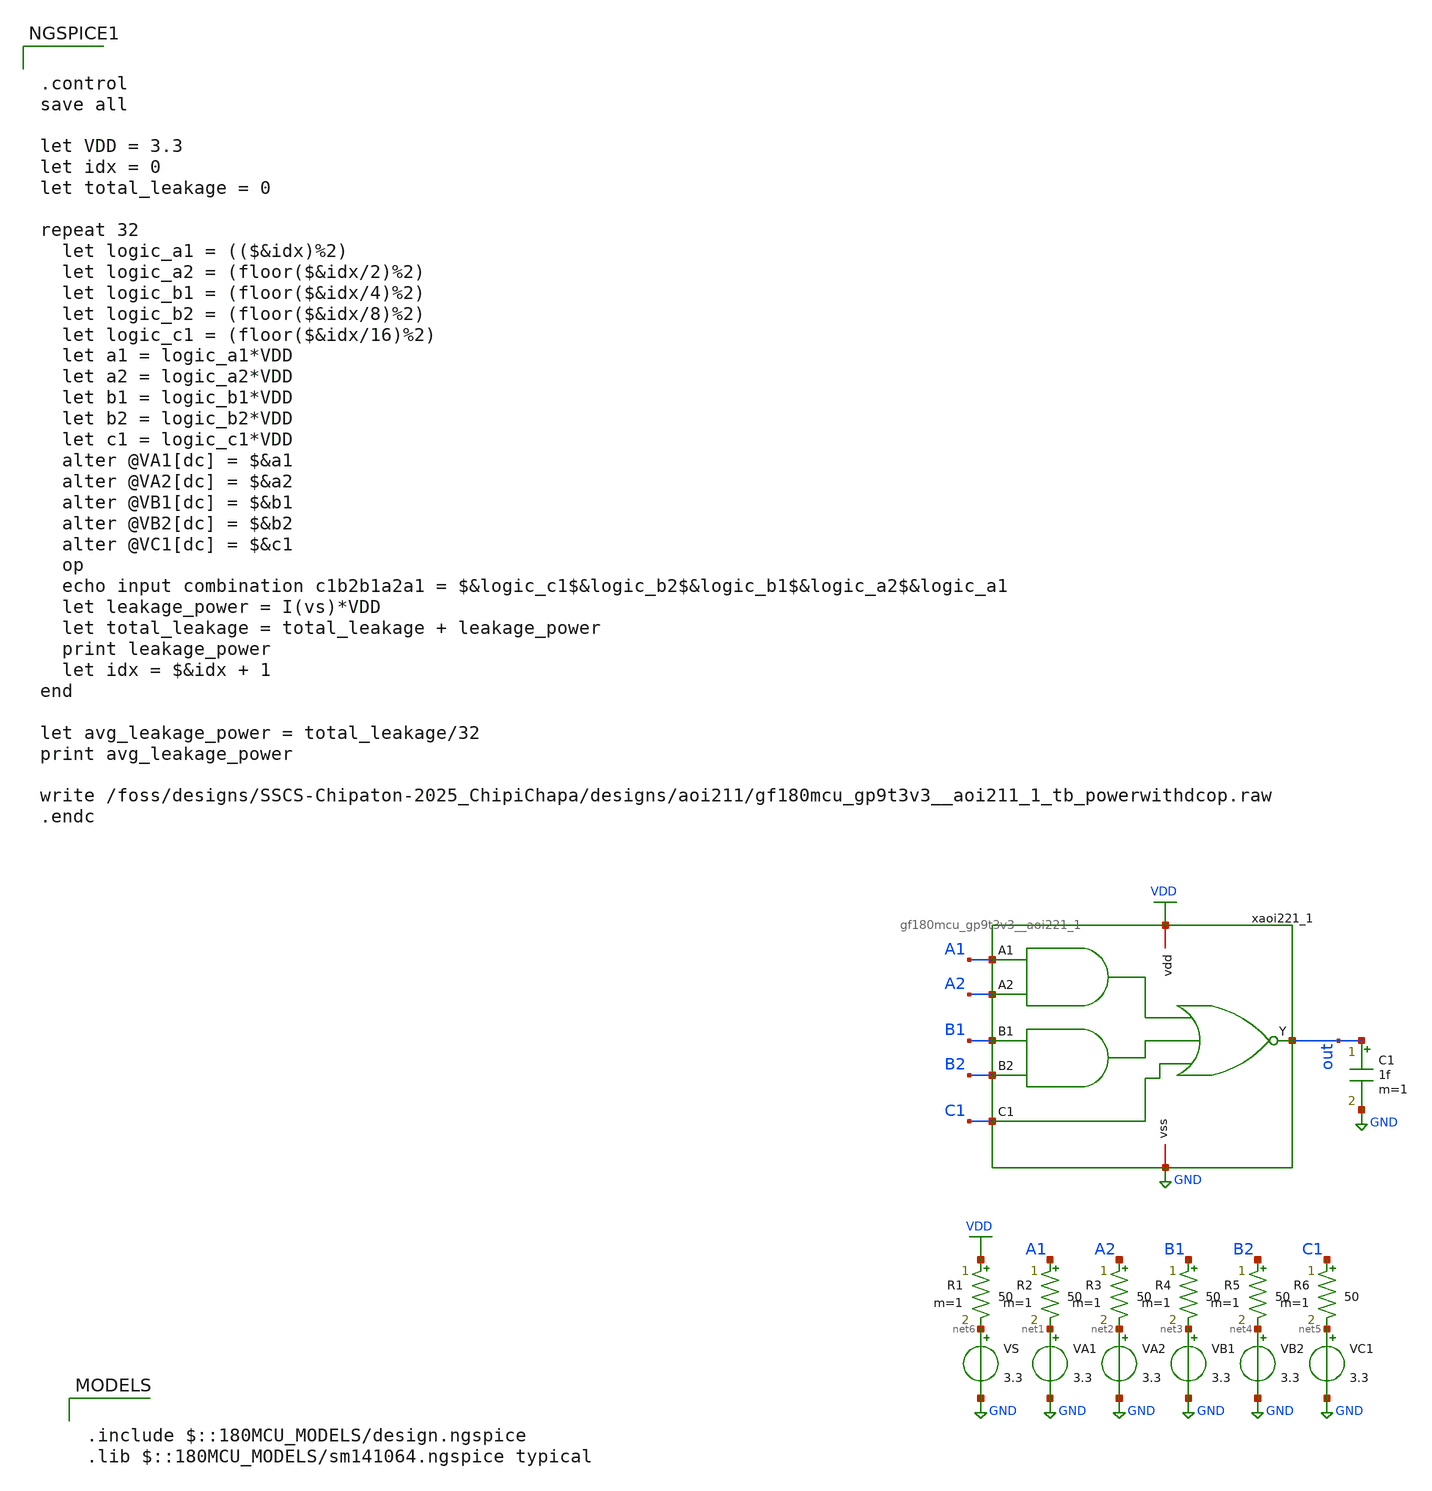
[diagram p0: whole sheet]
** sch_path: designs/aoi221/gf180mcu_gp9t3v3__aoi221_1_tb_power_with_dc_op.sch
**.subckt gf180mcu_gp9t3v3__aoi221_1_tb_power_with_dc_op
VA1 net1 GND 3.3
VA2 net2 GND 3.3
VB1 net3 GND 3.3
VB2 net4 GND 3.3
VC1 net5 GND 3.3
VS net6 GND 3.3
xaoi221_1 VDD out B1 A1 C1 B2 A2 GND gf180mcu_gp9t3v3__aoi221_1
C1 out GND 1f m=1
R1 VDD net6 50 m=1
R2 A1 net1 50 m=1
R3 A2 net2 50 m=1
R4 B1 net3 50 m=1
R5 B2 net4 50 m=1
R6 C1 net5 50 m=1
**** begin user architecture code

.include $::180MCU_MODELS/design.ngspice
.lib $::180MCU_MODELS/sm141064.ngspice typical



.control
save all

let VDD = 3.3
let idx = 0
let total_leakage = 0

repeat 32
  let logic_a1 = (($&idx)%2)
  let logic_a2 = (floor($&idx/2)%2)
  let logic_b1 = (floor($&idx/4)%2)
  let logic_b2 = (floor($&idx/8)%2)
  let logic_c1 = (floor($&idx/16)%2)
  let a1 = logic_a1*VDD
  let a2 = logic_a2*VDD
  let b1 = logic_b1*VDD
  let b2 = logic_b2*VDD
  let c1 = logic_c1*VDD
  alter @VA1[dc] = $&a1
  alter @VA2[dc] = $&a2
  alter @VB1[dc] = $&b1
  alter @VB2[dc] = $&b2
  alter @VC1[dc] = $&c1
  op
  echo input combination c1b2b1a2a1 = $&logic_c1$&logic_b2$&logic_b1$&logic_a2$&logic_a1
  let leakage_power = I(vs)*VDD
  let total_leakage = total_leakage + leakage_power
  print leakage_power
  let idx = $&idx + 1
end

let avg_leakage_power = total_leakage/32
print avg_leakage_power

write
+ /foss/designs/SSCS-Chipaton-2025_ChipiChapa/designs/aoi211/gf180mcu_gp9t3v3__aoi211_1_tb_powerwithdcop.raw
.endc


**** end user architecture code
**.ends

* expanding   symbol:  gf180mcu_gp9t3v3__aoi221_1.sym # of pins=8
** sym_path: designs/aoi221/gf180mcu_gp9t3v3__aoi221_1.sym
** sch_path: designs/aoi221/gf180mcu_gp9t3v3__aoi221_1.sch
.subckt gf180mcu_gp9t3v3__aoi221_1 vdd Y B1 A1 C1 B2 A2 vss
*.iopin vdd
*.iopin vss
*.ipin A1
*.ipin A2
*.ipin B2
*.ipin B1
*.ipin C1
*.opin Y
XM1 Y A1 net1 vss nfet_03v3 L=0.3u W=1u nf=1 ad='int((nf+1)/2) * W/nf * 0.18u' as='int((nf+2)/2) * W/nf * 0.18u'
+ pd='2*int((nf+1)/2) * (W/nf + 0.18u)' ps='2*int((nf+2)/2) * (W/nf + 0.18u)' nrd='0.18u / W' nrs='0.18u / W'
+ sa=0 sb=0 sd=0 m=1
XM2 net1 A2 vss vss nfet_03v3 L=0.3u W=1u nf=1 ad='int((nf+1)/2) * W/nf * 0.18u' as='int((nf+2)/2) * W/nf * 0.18u'
+ pd='2*int((nf+1)/2) * (W/nf + 0.18u)' ps='2*int((nf+2)/2) * (W/nf + 0.18u)' nrd='0.18u / W' nrs='0.18u / W'
+ sa=0 sb=0 sd=0 m=1
XM3 Y B1 net2 vss nfet_03v3 L=0.3u W=1u nf=1 ad='int((nf+1)/2) * W/nf * 0.18u' as='int((nf+2)/2) * W/nf * 0.18u'
+ pd='2*int((nf+1)/2) * (W/nf + 0.18u)' ps='2*int((nf+2)/2) * (W/nf + 0.18u)' nrd='0.18u / W' nrs='0.18u / W'
+ sa=0 sb=0 sd=0 m=1
XM4 net2 B2 vss vss nfet_03v3 L=0.3u W=1u nf=1 ad='int((nf+1)/2) * W/nf * 0.18u' as='int((nf+2)/2) * W/nf * 0.18u'
+ pd='2*int((nf+1)/2) * (W/nf + 0.18u)' ps='2*int((nf+2)/2) * (W/nf + 0.18u)' nrd='0.18u / W' nrs='0.18u / W'
+ sa=0 sb=0 sd=0 m=1
XM5 Y C1 vss vss nfet_03v3 L=0.3u W=0.5u nf=1 ad='int((nf+1)/2) * W/nf * 0.18u' as='int((nf+2)/2) * W/nf * 0.18u'
+ pd='2*int((nf+1)/2) * (W/nf + 0.18u)' ps='2*int((nf+2)/2) * (W/nf + 0.18u)' nrd='0.18u / W' nrs='0.18u / W'
+ sa=0 sb=0 sd=0 m=1
XM6 net4 A1 vdd vdd pfet_03v3 L=0.3u W=2.25u nf=1 ad='int((nf+1)/2) * W/nf * 0.18u' as='int((nf+2)/2) * W/nf * 0.18u'
+ pd='2*int((nf+1)/2) * (W/nf + 0.18u)' ps='2*int((nf+2)/2) * (W/nf + 0.18u)' nrd='0.18u / W' nrs='0.18u / W'
+ sa=0 sb=0 sd=0 m=1
XM7 net4 A2 vdd vdd pfet_03v3 L=0.3u W=2.25u nf=1 ad='int((nf+1)/2) * W/nf * 0.18u' as='int((nf+2)/2) * W/nf * 0.18u'
+ pd='2*int((nf+1)/2) * (W/nf + 0.18u)' ps='2*int((nf+2)/2) * (W/nf + 0.18u)' nrd='0.18u / W' nrs='0.18u / W'
+ sa=0 sb=0 sd=0 m=1
XM8 net3 B1 net4 vdd pfet_03v3 L=0.3u W=2.25u nf=1 ad='int((nf+1)/2) * W/nf * 0.18u' as='int((nf+2)/2) * W/nf * 0.18u'
+ pd='2*int((nf+1)/2) * (W/nf + 0.18u)' ps='2*int((nf+2)/2) * (W/nf + 0.18u)' nrd='0.18u / W' nrs='0.18u / W'
+ sa=0 sb=0 sd=0 m=1
XM9 net3 B2 net4 vdd pfet_03v3 L=0.3u W=2.25u nf=1 ad='int((nf+1)/2) * W/nf * 0.18u' as='int((nf+2)/2) * W/nf * 0.18u'
+ pd='2*int((nf+1)/2) * (W/nf + 0.18u)' ps='2*int((nf+2)/2) * (W/nf + 0.18u)' nrd='0.18u / W' nrs='0.18u / W'
+ sa=0 sb=0 sd=0 m=1
XM10 Y C1 net3 vdd pfet_03v3 L=0.3u W=2.25u nf=1 ad='int((nf+1)/2) * W/nf * 0.18u' as='int((nf+2)/2) * W/nf * 0.18u'
+ pd='2*int((nf+1)/2) * (W/nf + 0.18u)' ps='2*int((nf+2)/2) * (W/nf + 0.18u)' nrd='0.18u / W' nrs='0.18u / W'
+ sa=0 sb=0 sd=0 m=1
.ends

.GLOBAL VDD
.GLOBAL GND
.end
